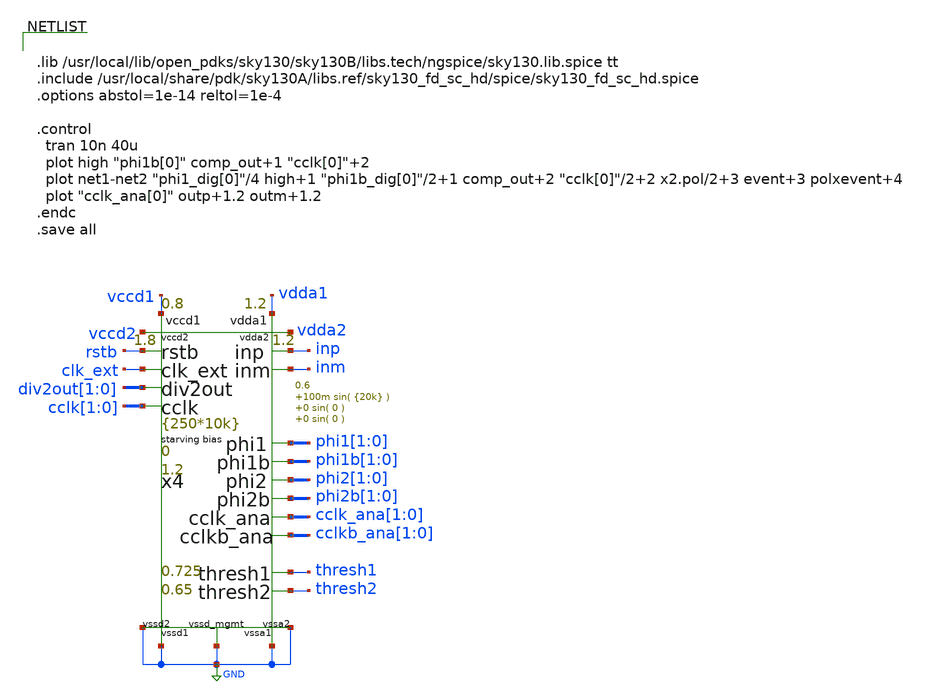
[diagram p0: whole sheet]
** sch_path: xschem/test_bench/clkgen_tb.sch
**.subckt clkgen_tb
x4 thresh1 thresh2 inp inm clk_ext rstb phi1[1] phi1[0] phi1b[1] phi1b[0] phi2[1] phi2[0] phi2b[1] phi2b[0]
+ cclk_ana[1] cclk_ana[0] cclkb_ana[1] cclkb_ana[0] div2out[1] div2out[0] cclk[1] cclk[0] vdda1 vccd1 vccd2
+ vdda2 GND GND GND GND GND risc_signals p_vdda1=1.2 p_vdda2=1.2 p_vccd1=0.8 p_vccd2=1.8 p_vccd_mgmt=1.8
+ p_fclk={250*10k} p_duty_cycle=0.5 p_rstb_delay={1.5/p_fclk} p_rstb_tr=5n p_thresh1=0.725 p_thresh2=0.65
+ p_vpb=0 p_vnb=1.2 p_vcm=0.6 p_amp1=100m p_f1={20k} p_amp2=0 p_f2=0 p_amp3=0 p_f3=0
**** begin user architecture code


.lib /usr/local/lib/open_pdks/sky130/sky130B/libs.tech/ngspice/sky130.lib.spice tt
.include /usr/local/share/pdk/sky130A/libs.ref/sky130_fd_sc_hd/spice/sky130_fd_sc_hd.spice
.options abstol=1e-14 reltol=1e-4

.control
  tran 10n 40u
  plot high "phi1b[0]" comp_out+1 "cclk[0]"+2
  plot net1-net2 "phi1_dig[0]"/4 high+1 "phi1b_dig[0]"/2+1 comp_out+2 "cclk[0]"/2+2 x2.pol/2+3
+ event+3 polxevent+4
  plot "cclk_ana[0]" outp+1.2 outm+1.2
.endc
.save all


**** end user architecture code
**.ends
.GLOBAL GND
.end
